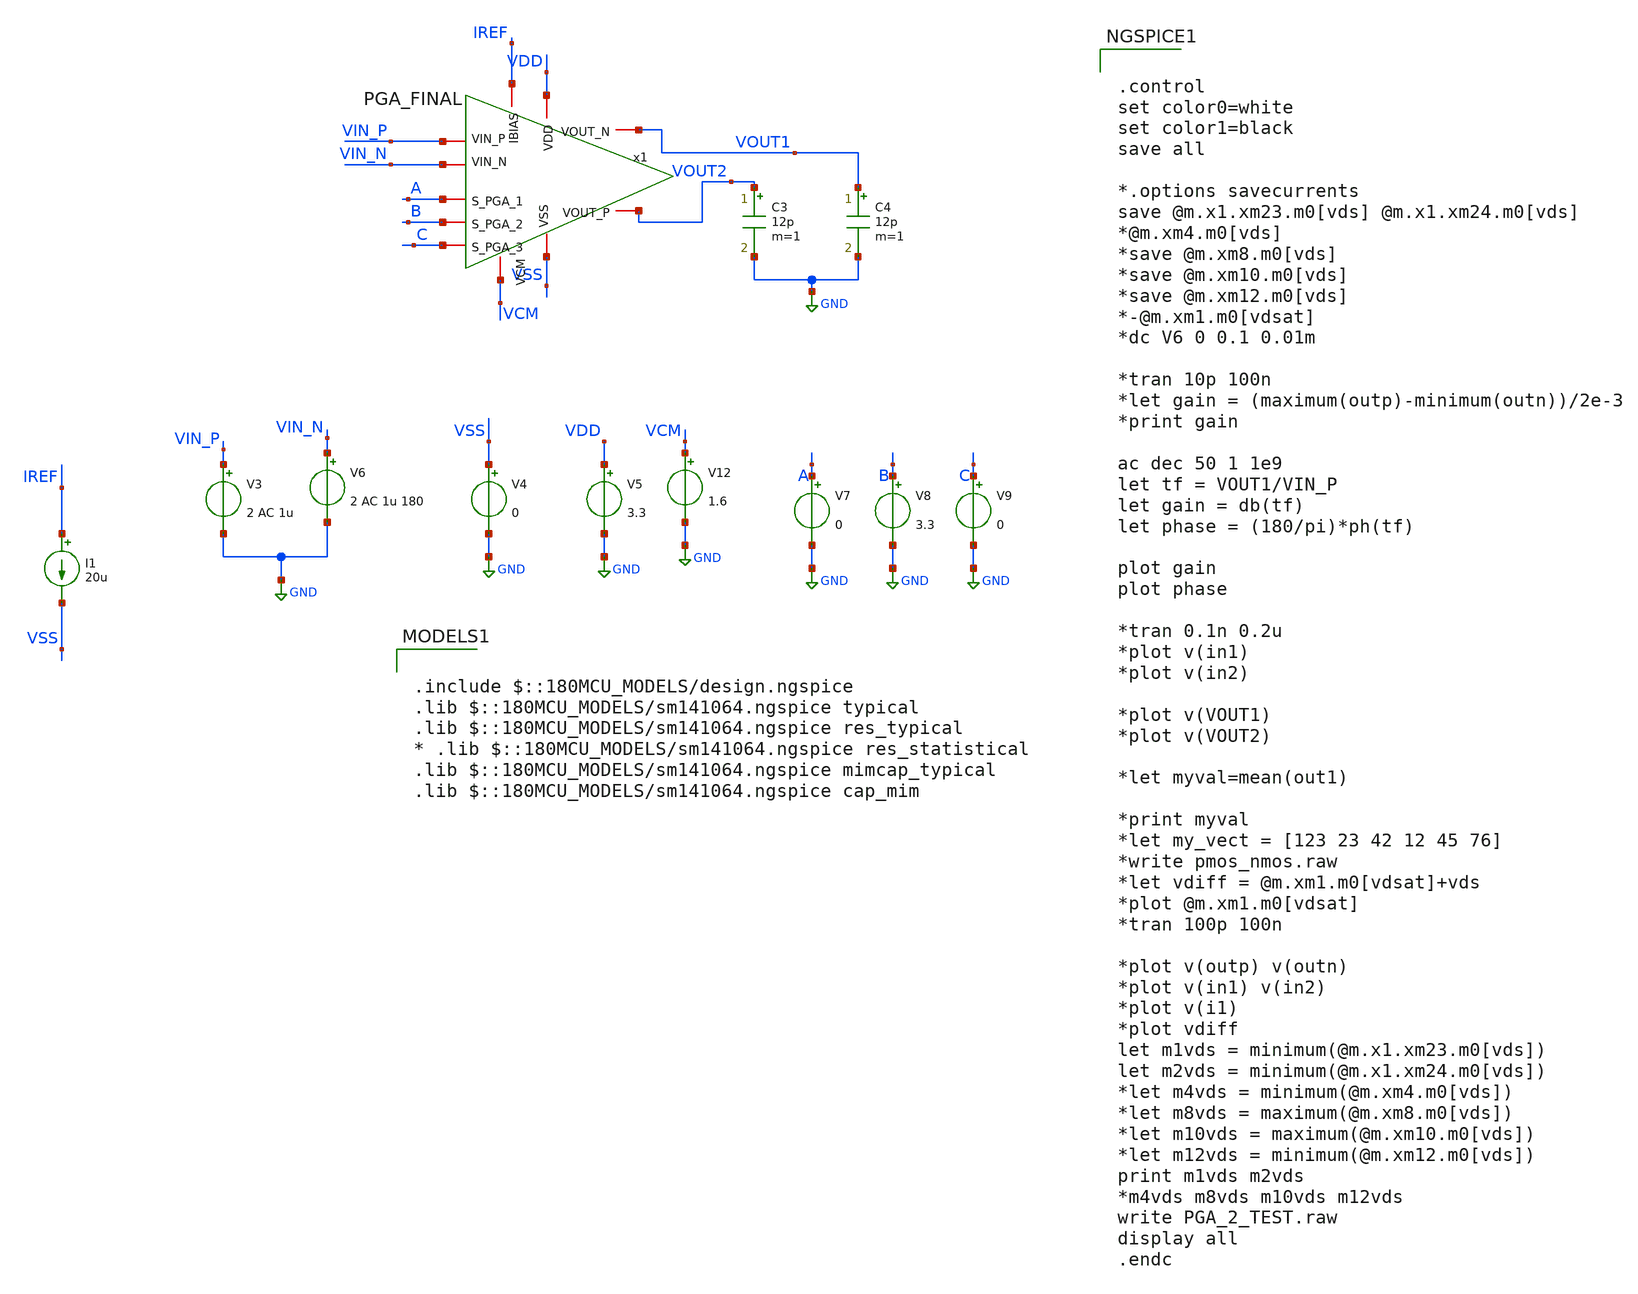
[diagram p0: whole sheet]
** sch_path: AWG_OUTPUT_AND_MUX_PAKISTAN_05/xschem/PGA_FINAL_TB.sch
**.subckt PGA_FINAL_TB
V4 VSS GND 0
V5 VDD GND 3.3
I1 IREF VSS 20u
V7 A GND 0
V8 B GND 3.3
V9 C GND 0
V12 VCM GND 1.6
V3 VIN_P GND 2 AC 1u
V6 VIN_N GND 2 AC 1u 180
C3 VOUT2 GND 12p m=1
C4 VOUT1 GND 12p m=1
x1 VOUT1 VIN_P VDD A VSS VIN_N B VOUT2 C IREF VCM PGA_FINAL
**** begin user architecture code


.control
set color0=white
set color1=black
save all

*.options savecurrents
save @m.x1.xm23.m0[vds] @m.x1.xm24.m0[vds]
*@m.xm4.m0[vds]
*save @m.xm8.m0[vds]
*save @m.xm10.m0[vds]
*save @m.xm12.m0[vds]
*-@m.xm1.m0[vdsat]
*dc V6 0 0.1 0.01m

*tran 10p 100n
*let gain = (maximum(outp)-minimum(outn))/2e-3
*print gain

ac dec 50 1 1e9
let tf = VOUT1/VIN_P
let gain = db(tf)
let phase = (180/pi)*ph(tf)

plot gain
plot phase

*tran 0.1n 0.2u
*plot v(in1)
*plot v(in2)

*plot v(VOUT1)
*plot v(VOUT2)

*let myval=mean(out1)

*print myval
*let my_vect = [123 23 42 12 45 76]
*write pmos_nmos.raw
*let vdiff = @m.xm1.m0[vdsat]+vds
*plot @m.xm1.m0[vdsat]
*tran 100p 100n

*plot v(outp) v(outn)
*plot v(in1) v(in2)
*plot v(i1)
*plot vdiff
let m1vds = minimum(@m.x1.xm23.m0[vds])
let m2vds = minimum(@m.x1.xm24.m0[vds])
*let m4vds = minimum(@m.xm4.m0[vds])
*let m8vds = maximum(@m.xm8.m0[vds])
*let m10vds = maximum(@m.xm10.m0[vds])
*let m12vds = minimum(@m.xm12.m0[vds])
print m1vds m2vds
*m4vds m8vds m10vds m12vds
write PGA_2_TEST.raw
display all
.endc



.include $::180MCU_MODELS/design.ngspice
.lib $::180MCU_MODELS/sm141064.ngspice typical
.lib $::180MCU_MODELS/sm141064.ngspice res_typical
* .lib $::180MCU_MODELS/sm141064.ngspice res_statistical
.lib $::180MCU_MODELS/sm141064.ngspice mimcap_typical
.lib $::180MCU_MODELS/sm141064.ngspice cap_mim

**** end user architecture code
**.ends
.GLOBAL GND
.end
